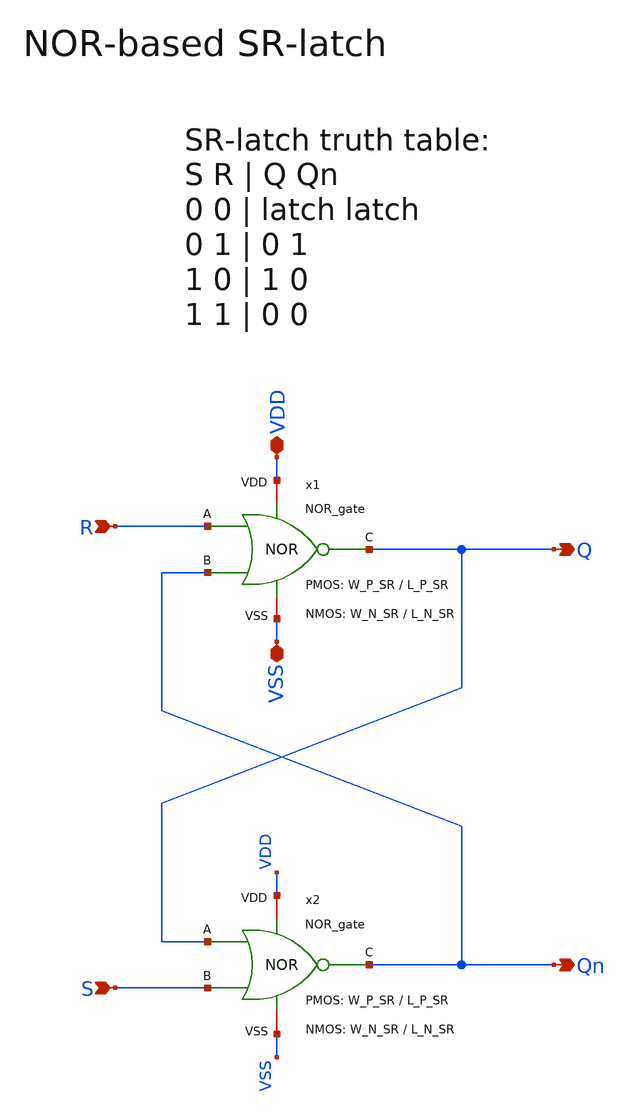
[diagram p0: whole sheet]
** sch_path: SG13G2_ATBS-ADC-main/xschem/comparator/SR_latch/SR_latch.sch
**.subckt SR_latch VDD Q VSS S R Qn
*.iopin VDD
*.opin Q
*.iopin VSS
*.ipin S
*.ipin R
*.opin Qn
x1 VDD Q R Qn VSS NOR_gate W_P=W_P_SR L_P=L_P_SR W_N=W_N_SR L_N=L_N_SR
x2 VDD Qn Q S VSS NOR_gate W_P=W_P_SR L_P=L_P_SR W_N=W_N_SR L_N=L_N_SR
**.ends

* expanding   symbol:  comparator/NOR_gate/NOR_gate.sym # of pins=5
** sym_path: SG13G2_ATBS-ADC-main/xschem/comparator/NOR_gate/NOR_gate.sym
** sch_path: SG13G2_ATBS-ADC-main/xschem/comparator/NOR_gate/NOR_gate.sch
.subckt NOR_gate VDD C A B VSS  W_P=1.0u L_P=0.13u W_N=0.5u L_N=0.13u
*.iopin VDD
*.opin C
*.iopin VSS
*.ipin A
*.ipin B
XM1 C A VSS VSS sg13_lv_nmos w=W_N l=L_N ng=1 m=1 mm_ok=1
XM2 C B VSS VSS sg13_lv_nmos w=W_N l=L_N ng=1 m=1 mm_ok=1
XM3 C B net1 VDD sg13_lv_pmos w=W_P l=L_P ng=1 m=1 mm_ok=1
XM4 net1 A VDD VDD sg13_lv_pmos w=W_P l=L_P ng=1 m=1 mm_ok=1
XM5 C A net2 VDD sg13_lv_pmos w=W_P l=L_P ng=1 m=1 mm_ok=1
XM6 net2 B VDD VDD sg13_lv_pmos w=W_P l=L_P ng=1 m=1 mm_ok=1
.ends

.end
